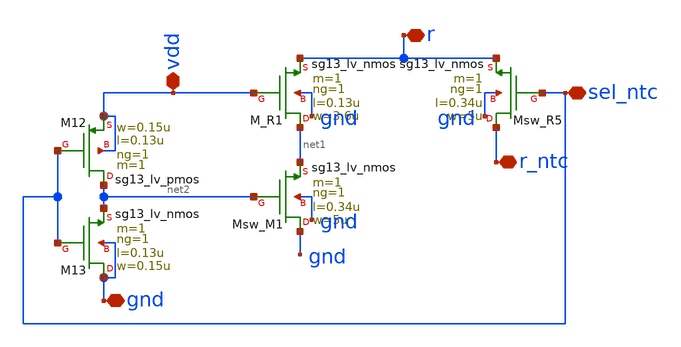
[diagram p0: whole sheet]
** sch_path: Enfoque_B/xschem/celdas/sel_r_ntc.sch
**.subckt sel_r_ntc sel_ntc r_ntc r vdd gnd
*.iopin sel_ntc
*.iopin r_ntc
*.iopin r
*.iopin vdd
*.iopin gnd
XMsw_R5 r_ntc sel_ntc r gnd sg13_lv_nmos w=5u l=0.34u ng=1 m=1 mm_ok=1
XM_R1 net1 vdd r gnd sg13_lv_nmos w=3.6u l=0.13u ng=1 m=1 mm_ok=1
XMsw_M1 gnd net2 net1 gnd sg13_lv_nmos w=5u l=0.34u ng=1 m=1 mm_ok=1
XM12 net2 sel_ntc vdd vdd sg13_lv_pmos w=0.15u l=0.13u ng=1 m=1 mm_ok=1
XM13 gnd sel_ntc net2 gnd sg13_lv_nmos w=0.15u l=0.13u ng=1 m=1 mm_ok=1
**.ends
.end
